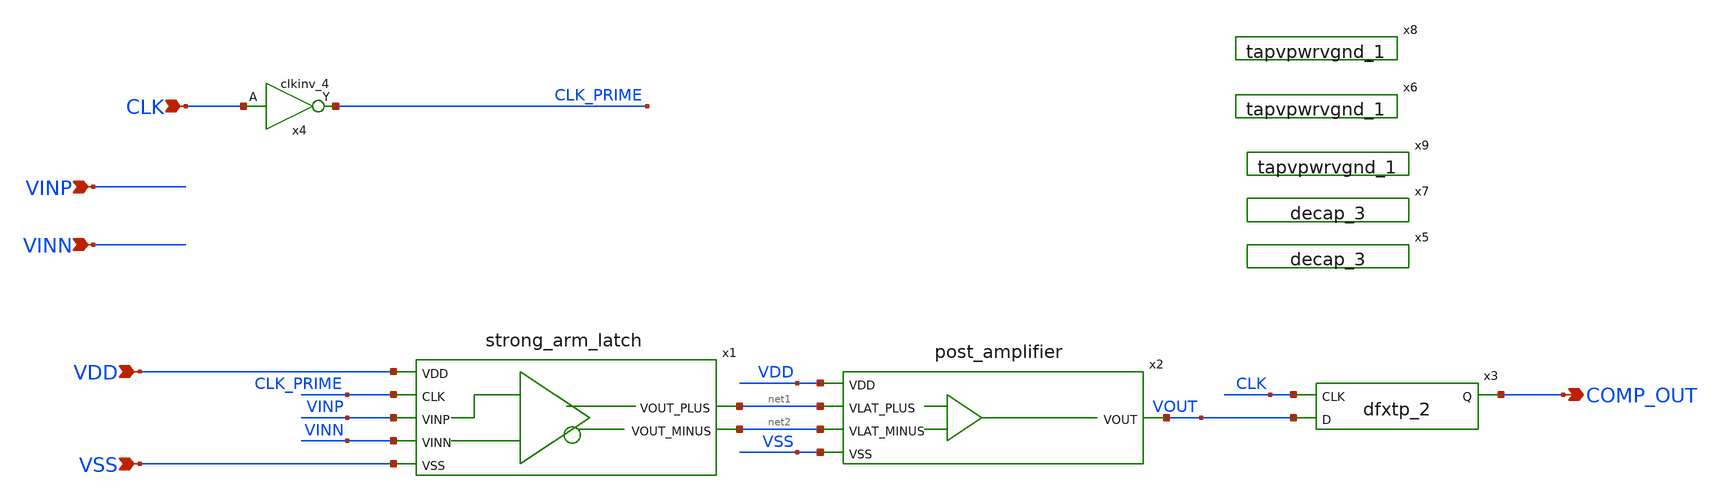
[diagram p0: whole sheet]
** sch_path: xschem/flash_converter/high_speed_comp_top.sch
**.subckt high_speed_comp_top VINP VINN CLK COMP_OUT VDD VSS
*.ipin VINP
*.ipin VINN
*.ipin CLK
*.opin COMP_OUT
*.ipin VDD
*.ipin VSS
x1 VDD CLK_PRIME net1 net2 VSS VINP VINN strong_arm_latch
x2 VDD net1 net2 VOUT VSS post_amplifier
x3 CLK VOUT VSS VSS VDD VDD COMP_OUT sky130_fd_sc_hd__dfxtp_2
x4 CLK VSS VSS VDD VDD CLK_PRIME sky130_fd_sc_hd__clkinv_4
x5 VSS VSS VDD VDD sky130_fd_sc_hd__decap_3
x7 VSS VSS VDD VDD sky130_fd_sc_hd__decap_3
x9 VSS VDD sky130_fd_sc_hd__tapvpwrvgnd_1
x6 VSS VDD sky130_fd_sc_hd__tapvpwrvgnd_1
x8 VSS VDD sky130_fd_sc_hd__tapvpwrvgnd_1
**.ends

* expanding   symbol:  strong_arm_latch.sym # of pins=7
** sym_path: xschem/flash_converter/strong_arm_latch.sym
** sch_path: xschem/flash_converter/strong_arm_latch.sch
.subckt strong_arm_latch VDD CLK VOUT_PLUS VOUT_MINUS VSS VINP VINN
*.ipin VSS
*.ipin VDD
*.ipin CLK
*.ipin VINP
*.ipin VINN
*.opin VOUT_MINUS
*.opin VOUT_PLUS
XM1 net2 VINP net1 VSS sky130_fd_pr__nfet_01v8_lvt L=1 W=5 nf=1 ad='int((nf+1)/2) * W/nf * 0.29' as='int((nf+2)/2) * W/nf * 0.29'
+ pd='2*int((nf+1)/2) * (W/nf + 0.29)' ps='2*int((nf+2)/2) * (W/nf + 0.29)' nrd='0.29 / W' nrs='0.29 / W'
+ sa=0 sb=0 sd=0 mult=1 m=1
XM2 net3 VINN net1 VSS sky130_fd_pr__nfet_01v8_lvt L=1 W=5 nf=1 ad='int((nf+1)/2) * W/nf * 0.29' as='int((nf+2)/2) * W/nf * 0.29'
+ pd='2*int((nf+1)/2) * (W/nf + 0.29)' ps='2*int((nf+2)/2) * (W/nf + 0.29)' nrd='0.29 / W' nrs='0.29 / W'
+ sa=0 sb=0 sd=0 mult=1 m=1
XM3 net1 CLK VSS VSS sky130_fd_pr__nfet_01v8_lvt L=1 W=5 nf=1 ad='int((nf+1)/2) * W/nf * 0.29' as='int((nf+2)/2) * W/nf * 0.29'
+ pd='2*int((nf+1)/2) * (W/nf + 0.29)' ps='2*int((nf+2)/2) * (W/nf + 0.29)' nrd='0.29 / W' nrs='0.29 / W'
+ sa=0 sb=0 sd=0 mult=1 m=1
XM4 VOUT_PLUS VOUT_MINUS net2 VSS sky130_fd_pr__nfet_01v8 L=0.15 W=1 nf=1 ad='int((nf+1)/2) * W/nf * 0.29'
+ as='int((nf+2)/2) * W/nf * 0.29' pd='2*int((nf+1)/2) * (W/nf + 0.29)' ps='2*int((nf+2)/2) * (W/nf + 0.29)'
+ nrd='0.29 / W' nrs='0.29 / W' sa=0 sb=0 sd=0 mult=1 m=1
XM5 VOUT_MINUS VOUT_PLUS net3 VSS sky130_fd_pr__nfet_01v8 L=0.15 W=1 nf=1 ad='int((nf+1)/2) * W/nf * 0.29'
+ as='int((nf+2)/2) * W/nf * 0.29' pd='2*int((nf+1)/2) * (W/nf + 0.29)' ps='2*int((nf+2)/2) * (W/nf + 0.29)'
+ nrd='0.29 / W' nrs='0.29 / W' sa=0 sb=0 sd=0 mult=1 m=1
XM6 VOUT_PLUS VOUT_MINUS VDD VDD sky130_fd_pr__pfet_01v8 L=0.15 W=1 nf=1 ad='int((nf+1)/2) * W/nf * 0.29'
+ as='int((nf+2)/2) * W/nf * 0.29' pd='2*int((nf+1)/2) * (W/nf + 0.29)' ps='2*int((nf+2)/2) * (W/nf + 0.29)'
+ nrd='0.29 / W' nrs='0.29 / W' sa=0 sb=0 sd=0 mult=1 m=1
XM7 VOUT_MINUS VOUT_PLUS VDD VDD sky130_fd_pr__pfet_01v8 L=0.15 W=1 nf=1 ad='int((nf+1)/2) * W/nf * 0.29'
+ as='int((nf+2)/2) * W/nf * 0.29' pd='2*int((nf+1)/2) * (W/nf + 0.29)' ps='2*int((nf+2)/2) * (W/nf + 0.29)'
+ nrd='0.29 / W' nrs='0.29 / W' sa=0 sb=0 sd=0 mult=1 m=1
XM8 VOUT_PLUS CLK VDD VDD sky130_fd_pr__pfet_01v8 L=0.15 W=10 nf=1 ad='int((nf+1)/2) * W/nf * 0.29' as='int((nf+2)/2) * W/nf * 0.29'
+ pd='2*int((nf+1)/2) * (W/nf + 0.29)' ps='2*int((nf+2)/2) * (W/nf + 0.29)' nrd='0.29 / W' nrs='0.29 / W'
+ sa=0 sb=0 sd=0 mult=1 m=1
XM9 net2 CLK VDD VDD sky130_fd_pr__pfet_01v8 L=0.15 W=10 nf=1 ad='int((nf+1)/2) * W/nf * 0.29' as='int((nf+2)/2) * W/nf * 0.29'
+ pd='2*int((nf+1)/2) * (W/nf + 0.29)' ps='2*int((nf+2)/2) * (W/nf + 0.29)' nrd='0.29 / W' nrs='0.29 / W'
+ sa=0 sb=0 sd=0 mult=1 m=1
XM10 VOUT_MINUS CLK VDD VDD sky130_fd_pr__pfet_01v8 L=0.15 W=10 nf=1 ad='int((nf+1)/2) * W/nf * 0.29'
+ as='int((nf+2)/2) * W/nf * 0.29' pd='2*int((nf+1)/2) * (W/nf + 0.29)' ps='2*int((nf+2)/2) * (W/nf + 0.29)'
+ nrd='0.29 / W' nrs='0.29 / W' sa=0 sb=0 sd=0 mult=1 m=1
XM11 net3 CLK VDD VDD sky130_fd_pr__pfet_01v8 L=0.15 W=10 nf=1 ad='int((nf+1)/2) * W/nf * 0.29' as='int((nf+2)/2) * W/nf * 0.29'
+ pd='2*int((nf+1)/2) * (W/nf + 0.29)' ps='2*int((nf+2)/2) * (W/nf + 0.29)' nrd='0.29 / W' nrs='0.29 / W'
+ sa=0 sb=0 sd=0 mult=1 m=1
.ends


* expanding   symbol:  post_amplifier.sym # of pins=5
** sym_path: xschem/flash_converter/post_amplifier.sym
** sch_path: xschem/flash_converter/post_amplifier.sch
.subckt post_amplifier VDD VLAT_PLUS VLAT_MINUS VOUT VSS
*.ipin VLAT_PLUS
*.ipin VLAT_MINUS
*.ipin VDD
*.ipin VSS
*.opin VOUT
XM1 net1 VLAT_PLUS net4 VSS sky130_fd_pr__nfet_01v8 L=0.15 W=1 nf=1 ad='int((nf+1)/2) * W/nf * 0.29'
+ as='int((nf+2)/2) * W/nf * 0.29' pd='2*int((nf+1)/2) * (W/nf + 0.29)' ps='2*int((nf+2)/2) * (W/nf + 0.29)'
+ nrd='0.29 / W' nrs='0.29 / W' sa=0 sb=0 sd=0 mult=1 m=1
XM2 net3 VLAT_MINUS net4 VSS sky130_fd_pr__nfet_01v8 L=0.15 W=1 nf=1 ad='int((nf+1)/2) * W/nf * 0.29'
+ as='int((nf+2)/2) * W/nf * 0.29' pd='2*int((nf+1)/2) * (W/nf + 0.29)' ps='2*int((nf+2)/2) * (W/nf + 0.29)'
+ nrd='0.29 / W' nrs='0.29 / W' sa=0 sb=0 sd=0 mult=1 m=1
XM3 net4 net1 VSS VSS sky130_fd_pr__nfet_01v8 L=0.15 W=1 nf=1 ad='int((nf+1)/2) * W/nf * 0.29' as='int((nf+2)/2) * W/nf * 0.29'
+ pd='2*int((nf+1)/2) * (W/nf + 0.29)' ps='2*int((nf+2)/2) * (W/nf + 0.29)' nrd='0.29 / W' nrs='0.29 / W'
+ sa=0 sb=0 sd=0 mult=1 m=1
XM4 net1 VLAT_PLUS net2 VDD sky130_fd_pr__pfet_01v8 L=0.15 W=1 nf=1 ad='int((nf+1)/2) * W/nf * 0.29'
+ as='int((nf+2)/2) * W/nf * 0.29' pd='2*int((nf+1)/2) * (W/nf + 0.29)' ps='2*int((nf+2)/2) * (W/nf + 0.29)'
+ nrd='0.29 / W' nrs='0.29 / W' sa=0 sb=0 sd=0 mult=1 m=1
XM5 net3 VLAT_MINUS net2 VDD sky130_fd_pr__pfet_01v8 L=0.15 W=1 nf=1 ad='int((nf+1)/2) * W/nf * 0.29'
+ as='int((nf+2)/2) * W/nf * 0.29' pd='2*int((nf+1)/2) * (W/nf + 0.29)' ps='2*int((nf+2)/2) * (W/nf + 0.29)'
+ nrd='0.29 / W' nrs='0.29 / W' sa=0 sb=0 sd=0 mult=1 m=1
XM6 net2 net1 VDD VDD sky130_fd_pr__pfet_01v8 L=0.15 W=1 nf=1 ad='int((nf+1)/2) * W/nf * 0.29' as='int((nf+2)/2) * W/nf * 0.29'
+ pd='2*int((nf+1)/2) * (W/nf + 0.29)' ps='2*int((nf+2)/2) * (W/nf + 0.29)' nrd='0.29 / W' nrs='0.29 / W'
+ sa=0 sb=0 sd=0 mult=1 m=1
XM7 VOUT net3 VSS VSS sky130_fd_pr__nfet_01v8 L=0.15 W=1 nf=1 ad='int((nf+1)/2) * W/nf * 0.29' as='int((nf+2)/2) * W/nf * 0.29'
+ pd='2*int((nf+1)/2) * (W/nf + 0.29)' ps='2*int((nf+2)/2) * (W/nf + 0.29)' nrd='0.29 / W' nrs='0.29 / W'
+ sa=0 sb=0 sd=0 mult=1 m=1
XM8 VOUT net3 VDD VDD sky130_fd_pr__pfet_01v8 L=0.15 W=1 nf=1 ad='int((nf+1)/2) * W/nf * 0.29' as='int((nf+2)/2) * W/nf * 0.29'
+ pd='2*int((nf+1)/2) * (W/nf + 0.29)' ps='2*int((nf+2)/2) * (W/nf + 0.29)' nrd='0.29 / W' nrs='0.29 / W'
+ sa=0 sb=0 sd=0 mult=1 m=1
.ends

.end
